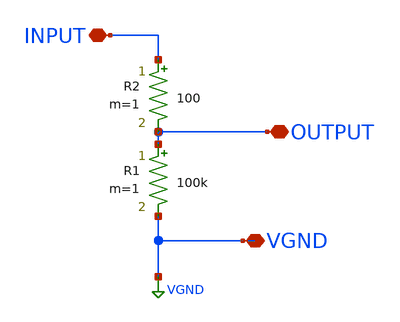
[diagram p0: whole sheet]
** sch_path: libs.ref/sky130_hilas_sc/xschem/sky130_hilas_polyresistorGND.sch
**.subckt sky130_hilas_polyresistorGND OUTPUT VGND INPUT
*.iopin OUTPUT
*.iopin VGND
*.iopin INPUT
R1 OUTPUT VGND 100k m=1
R2 INPUT OUTPUT 100 m=1
**.ends
.GLOBAL VGND
.end
